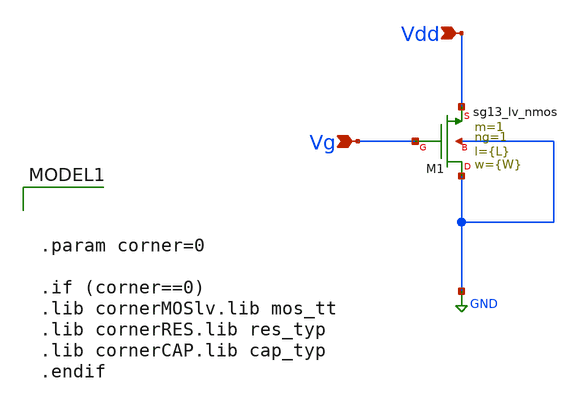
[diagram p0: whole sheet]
** sch_path: Tarea_1/xschem/gm_id-vs-Vov.sch
**.subckt gm_id-vs-Vov Vg Vdd
*.ipin Vg
*.ipin Vdd
XM1 GND Vg Vdd GND sg13_lv_nmos w={W} l={L} ng=1 m=1 mm_ok=1
**** begin user architecture code


.param corner=0

.if (corner==0)
.lib cornerMOSlv.lib mos_tt
.lib cornerRES.lib res_typ
.lib cornerCAP.lib cap_typ
.endif



.param L = 0.26u
.param W = 1.0u
vdd  Vdd 0 0.75
vgs vg 0 0.75
.control
save all
save @n.xm1.nsg13_lv_nmos[ids]
save @n.xm1.nsg13_lv_nmos[gm]
save @n.xm1.nsg13_lv_nmos[vth]
save @n.xm1.nsg13_lv_nmos[cgg]
save @n.xm1.nsg13_lv_nmos[cgsol]
save @n.xm1.nsg13_lv_nmos[cgdol]
save @n.xm1.nsg13_lv_nmos[vgs]
save @n.xm1.nsg13_lv_nmos[vdss]

dc vgs 0.1 1.2 0.01

let idn = @n.xm1.nsg13_lv_nmos[ids]
let gmn = @n.xm1.nsg13_lv_nmos[gm]
let vthn = @n.xm1.nsg13_lv_nmos[vth]
let vgsn = @n.xm1.nsg13_lv_nmos[vgs]


let vov = 2*idn/gmn
let vov2 = vgsn - vthn
*Vov teorico difiere demasiado con vov real
*Vov=2.38 cuando vgs=1.8, siendo que Vthn = .27
let gmoverId = gmn/idn

print vthn[0]
meas dc Vg_400 when gmoverID=4 CROSS=1
meas dc Vg_920 when gmoverID=9.2 CROSS=1
meas dc Vg_100 when gmoverID=10 CROSS=1
meas dc Vg_130 when gmoverID=13 CROSS=1

print vthn[0]-Vg_10
*(más fiable un measure?)
wrdata nmos_char_gmid-vov.raw gmoverID vov vov2
op
.endc


**** end user architecture code
**.ends
.GLOBAL GND
.end
